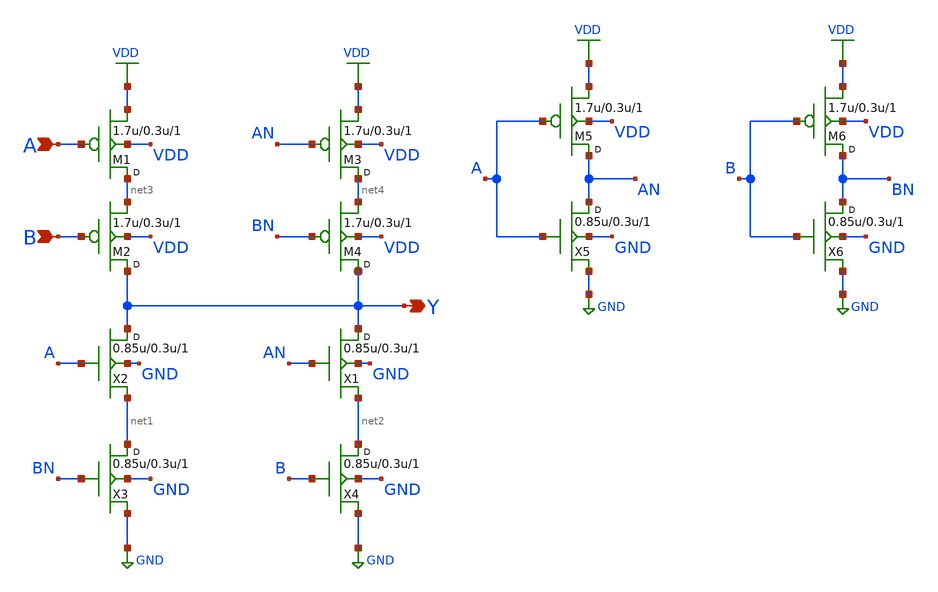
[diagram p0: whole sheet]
** sch_path: lib/12T/schematics/gf180mcu_osu_sc_xnor2_1.sch
**.subckt gf180mcu_osu_sc_xnor2_1 B A Y
*.ipin B
*.ipin A
*.opin Y
X2 Y A net1 GND nmos_3p3 w=0.85u l=0.3u m=1
X3 net1 BN GND GND nmos_3p3 w=0.85u l=0.3u m=1
X1 Y AN net2 GND nmos_3p3 w=0.85u l=0.3u m=1
X4 net2 B GND GND nmos_3p3 w=0.85u l=0.3u m=1
M1 net3 A VDD VDD pmos_3p3 w=1.7u l=0.3u m=1
M2 Y B net3 VDD pmos_3p3 w=1.7u l=0.3u m=1
M3 net4 AN VDD VDD pmos_3p3 w=1.7u l=0.3u m=1
M4 Y BN net4 VDD pmos_3p3 w=1.7u l=0.3u m=1
X5 AN A GND GND nmos_3p3 w=0.85u l=0.3u m=1
M5 AN A VDD VDD pmos_3p3 w=1.7u l=0.3u m=1
X6 BN B GND GND nmos_3p3 w=0.85u l=0.3u m=1
M6 BN B VDD VDD pmos_3p3 w=1.7u l=0.3u m=1
**** begin user architecture code


.inc "/import/yukari1/lrburle/OSU_180/char/techfiles/design.hspice"
.lib "/import/yukari1/lrburle/OSU_180/char/techfiles/sm141064.hspice" typical


**** end user architecture code
**.ends
.GLOBAL GND
.GLOBAL VDD
.end
